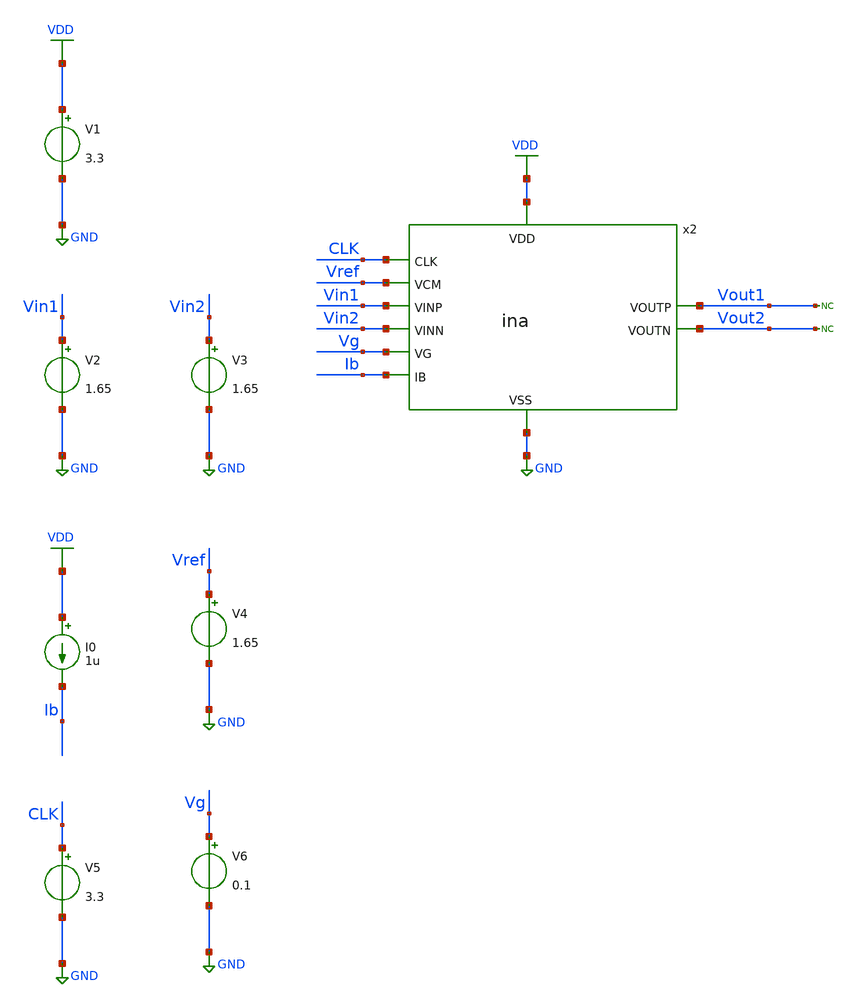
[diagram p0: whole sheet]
** sch_path: designs/libs/tb_ina/tb_ina_cmrr/tb_ina_cmrr.sch
**.subckt tb_ina_cmrr
V1 VDD GND 3.3
V2 Vin1 GND 1.65
V3 Vin2 GND 1.65
I0 VDD Ib 1u
V4 Vref GND 1.65
x2 Vg VDD Vin1 Vin2 CLK Vout1 Vout2 GND Vref Ib ina
V5 CLK GND 3.3
V6 Vg GND 0.1
* noconn Vout1
* noconn Vout2
**** begin user architecture code

.include $::180MCU_MODELS/design.ngspice
.lib $::180MCU_MODELS/sm141064.ngspice typical
.lib $::180MCU_MODELS/sm141064.ngspice cap_mim
.lib $::180MCU_MODELS/sm141064.ngspice moscap_typical
.lib $::180MCU_MODELS/sm141064.ngspice mimcap_typical
.lib $::180MCU_MODELS/sm141064.ngspice res_typical
* .lib $::180MCU_MODELS/sm141064.ngspice res_statistical
* ngspice commands




.control
save all

run
set color0 = white

*************************************
** PARAMETERS
*************************************

let Vdd  = 3.3
let Vcm  = 1.65
let Ibias = 2u
let Vg  = 0.1

*************************************
** CHOPPER PARAMETERS
*************************************

let fchop = 4k
let tper = 1/fchop
let ton = tper/2
let tr = 10n
let tf = 10n

*************************************
** COMMON SOURCES
*************************************

alter @V1[DC] = $&Vdd
alter @V2[DC] = $&Vcm
alter @V3[DC] = $&Vcm
alter @V4[DC] = $&Vcm
alter @I0[DC] = $&Ibias
alter @V5[PULSE] = [ 0 $&Vdd 0 $&tr $&tf $&ton $&tper 0 ]
alter @V6[DC] = $&Vg

*************************************
** DIFFERENTIAL GAIN
*************************************

alter @V2[ACMAG] = 0.5
alter @V3[ACMAG] = -0.5

ac dec 100 0.01 1G

write tb_ina_cmrr.raw
set appendwrite

*************************************
** COMMON-MODE GAIN
*************************************

alter @V2[ACMAG] = 1
alter @V3[ACMAG] = 1

ac dec 100 0.01 1G

write tb_ina_cmrr.raw
set appendwrite

*************************************
** MEASUREMENTS
*************************************

setplot new
setscale ac1.frequency
let Ad = (ac1.vout1-ac1.vout2)/(ac1.vin1-ac1.vin2)
let Acm = (ac2.vout1-ac2.vout2)/(ac1.vin1-ac1.vin2)
let cmrr = Ad/Acm
let cmrr_db = db(cmrr)

*************************************
** PLOTS
*************************************

plot cmrr_db xlog

*************************************
** SAVE
*************************************

write tb_ina_cmrr.raw
set appendwrite

.endc
* ngspice commands



**** end user architecture code
**.ends
.GLOBAL GND
.GLOBAL VDD
.end
